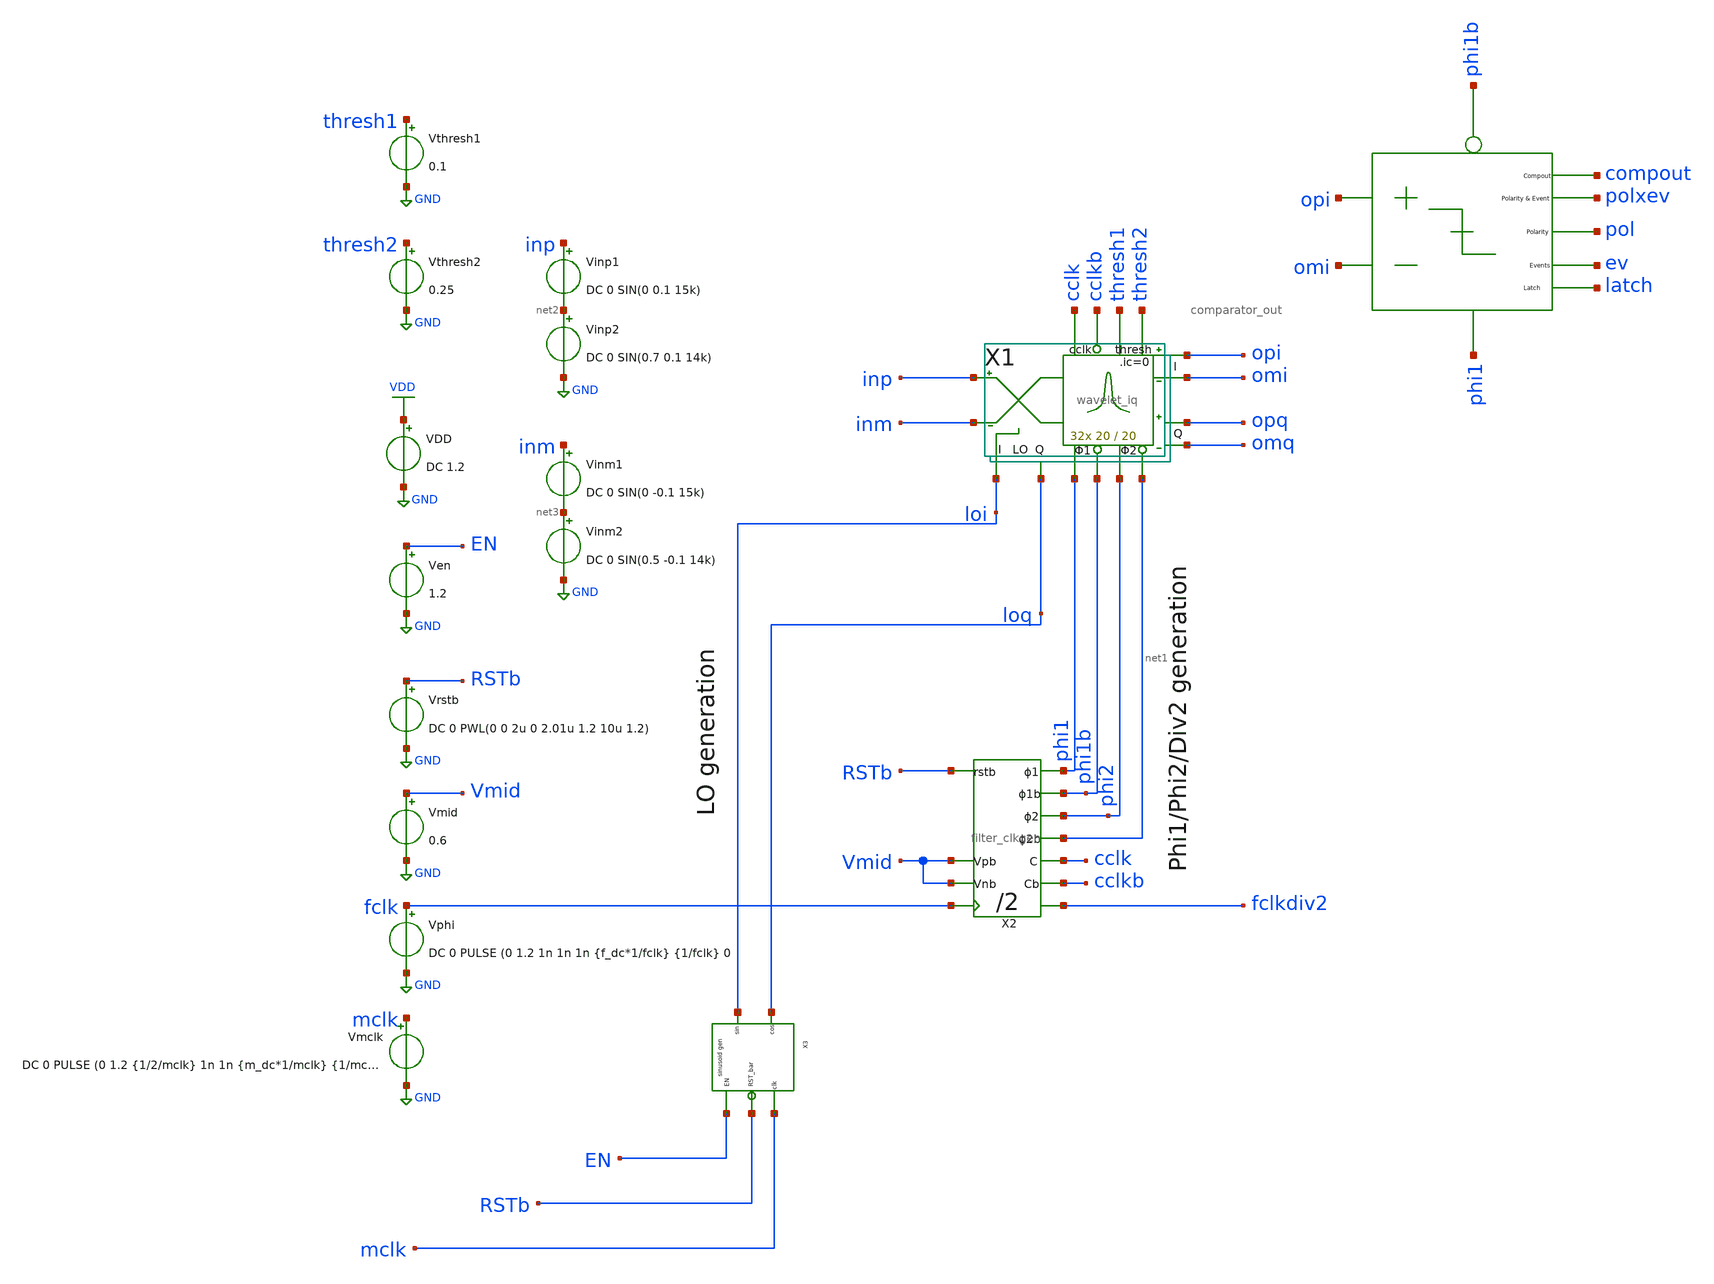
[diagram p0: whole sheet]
** sch_path: xschem/wavelet_channel/wavelet_iq_top_mini_tb.sch
**.subckt wavelet_iq_top_mini_tb
VDD VDD GND DC 1.2
Vphi fclk GND DC 0 PULSE (0 1.2 1n 1n 1n {f_dc*1/fclk} {1/fclk} 0
X1 inp opi phi1 phi2 inm omi loi loq opq omq net1 phi1b cclk cclkb thresh1 thresh2 wavelet_iq W=20
+ L=20
X2 RSTb fclk net1 phi2 phi1b phi1 cclkb cclk fclkdiv2 Vmid Vmid filter_clkgen
Ven EN GND 1.2
Vrstb RSTb GND DC 0 PWL(0 0 2u 0 2.01u 1.2 10u 1.2)
Vmid Vmid GND 0.6
Vmclk mclk GND DC 0 PULSE (0 1.2 {1/2/mclk} 1n 1n {m_dc*1/mclk} {1/mclk} 0
X3 EN RSTb mclk loi loq sinusoid_generator
Vthresh2 thresh2 GND 0.25
Vthresh1 thresh1 GND 0.1
Vinp1 inp net2 DC 0 SIN(0 0.1 15k)
Vinp2 net2 GND DC 0 SIN(0.7 0.1 14k)
Vinm1 inm net3 DC 0 SIN(0 -0.1 15k)
Vinm2 net3 GND DC 0 SIN(0.5 -0.1 14k)
x1 phi1b phi1 omi opi ev pol polxev compout latch comparator_out
**** begin user architecture code


.lib /home/sky/sky130A/libs.tech/ngspice/sky130.lib.spice tt
.include /home/sky/sky130A/libs.ref/sky130_fd_sc_lp/spice/sky130_fd_sc_lp.spice
.options abstol=1e-14 reltol=1e-4
.param ftest = 10k
.param Atest = 0.3
.param mclk={256*ftest}
.param m_dc = 0.5
* ratio of phi / lo clk:
.param ratio_fm = 1
.param f_dc = 0.5
.param fclk = {mclk*ratio_fm}
.param tau={1/4000}
.param tend={tau}
*start all caps with 0 charge:
*.ic included in cap symbols
.tran 1u {tend}
.save all


**** end user architecture code
**.ends
.GLOBAL VDD
.GLOBAL GND
.end
